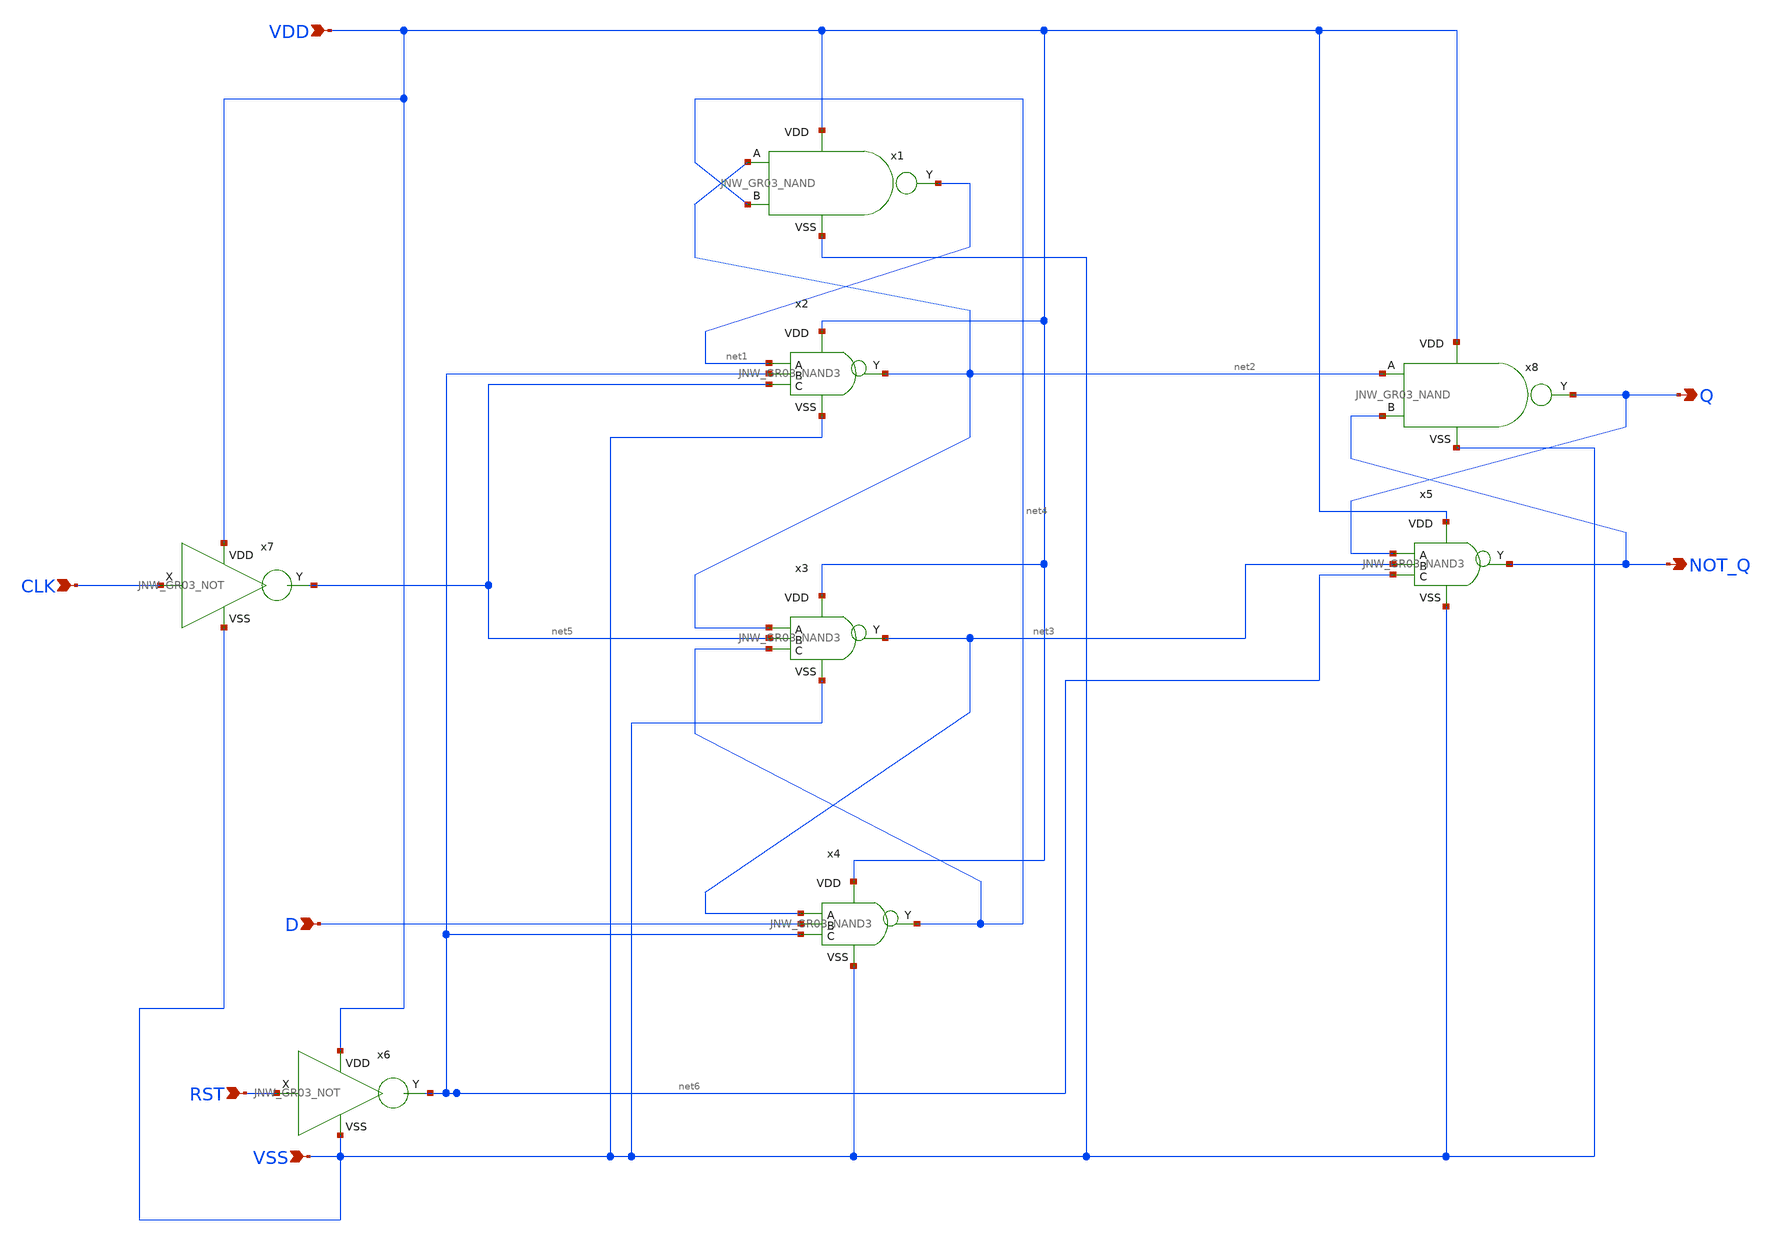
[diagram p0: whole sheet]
** sch_path: design/JNW_GR03_SKY130A/JNW_GR03_DFLIPFLOP_F_R.sch
**.subckt JNW_GR03_DFLIPFLOP_F_R Q RST CLK VSS D NOT_Q VDD
*.opin Q
*.ipin RST
*.ipin CLK
*.ipin VSS
*.ipin D
*.opin NOT_Q
*.ipin VDD
x1 VDD net1 net2 net4 VSS JNW_GR03_NAND
x8 VDD Q net2 NOT_Q VSS JNW_GR03_NAND
x2 VDD net1 net6 net2 net5 VSS JNW_GR03_NAND3
x3 VDD net2 net5 net3 net4 VSS JNW_GR03_NAND3
x4 VDD net3 D net4 net6 VSS JNW_GR03_NAND3
x5 VDD Q net3 NOT_Q net6 VSS JNW_GR03_NAND3
x6 VDD RST net6 VSS JNW_GR03_NOT
x7 VDD CLK net5 VSS JNW_GR03_NOT
**.ends
.end
